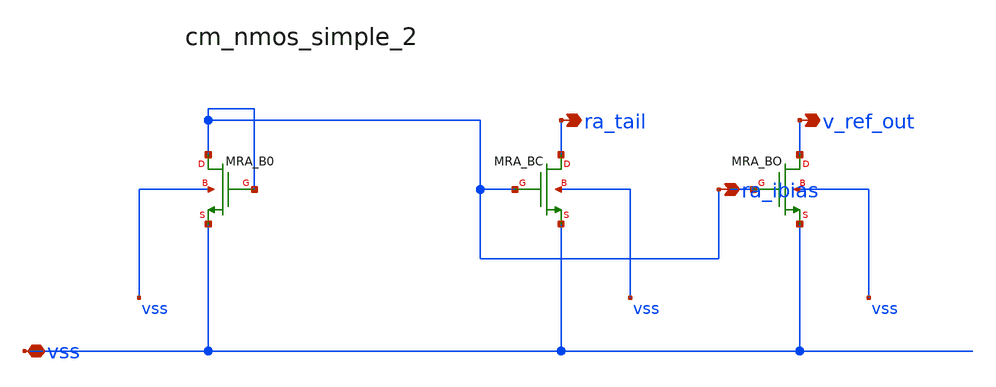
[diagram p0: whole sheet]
** sch_path: analog-db/raw/ldo_005_buffered_ref/hier/blocks/cm_nmos_simple_2.sch
**.subckt cm_nmos_simple_2 vss ra_ibias ra_tail v_ref_out
*.iopin vss
*.opin ra_ibias
*.opin ra_tail
*.opin v_ref_out
XMRA_B0 ra_ibias ra_ibias vss vss sg13_hv_nmos w=x_dut_xmra_b0_w l=x_dut_xmra_b0_l ng=1 m=1
XMRA_BC ra_tail ra_ibias vss vss sg13_hv_nmos w=x_dut_xmra_bc_w l=x_dut_xmra_bc_l ng=1 m=1
XMRA_BO v_ref_out ra_ibias vss vss sg13_hv_nmos w=x_dut_xmra_bo_w l=x_dut_xmra_bo_l ng=1 m=1
**.ends
.end
